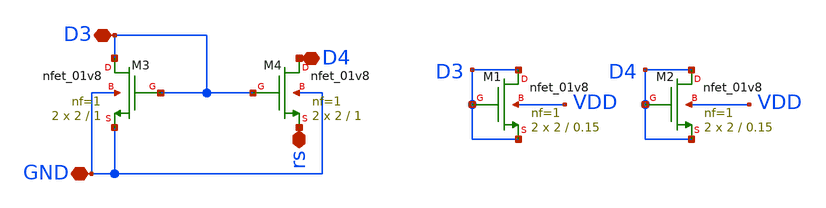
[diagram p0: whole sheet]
** sch_path: opamp/mag/untitled.sch
**.subckt untitled rs D3 GND D4
*.iopin rs
*.iopin D3
*.iopin GND
*.iopin D4
XM4 D4 D3 rs GND sky130_fd_pr__nfet_01v8 L=1 W=2 nf=1 ad='int((nf+1)/2) * W/nf * 0.29' as='int((nf+2)/2) * W/nf * 0.29'
+ pd='2*int((nf+1)/2) * (W/nf + 0.29)' ps='2*int((nf+2)/2) * (W/nf + 0.29)' nrd='0.29 / W' nrs='0.29 / W'
+ sa=0 sb=0 sd=0 mult=2 m=2
XM3 D3 D3 GND GND sky130_fd_pr__nfet_01v8 L=1 W=2 nf=1 ad='int((nf+1)/2) * W/nf * 0.29' as='int((nf+2)/2) * W/nf * 0.29'
+ pd='2*int((nf+1)/2) * (W/nf + 0.29)' ps='2*int((nf+2)/2) * (W/nf + 0.29)' nrd='0.29 / W' nrs='0.29 / W'
+ sa=0 sb=0 sd=0 mult=2 m=2
XM1 D3 D3 D3 VDD sky130_fd_pr__nfet_01v8 L=0.15 W=2 nf=1 ad='int((nf+1)/2) * W/nf * 0.29' as='int((nf+2)/2) * W/nf * 0.29'
+ pd='2*int((nf+1)/2) * (W/nf + 0.29)' ps='2*int((nf+2)/2) * (W/nf + 0.29)' nrd='0.29 / W' nrs='0.29 / W'
+ sa=0 sb=0 sd=0 mult=2 m=2
XM2 D4 D4 D4 VDD sky130_fd_pr__nfet_01v8 L=0.15 W=2 nf=1 ad='int((nf+1)/2) * W/nf * 0.29' as='int((nf+2)/2) * W/nf * 0.29'
+ pd='2*int((nf+1)/2) * (W/nf + 0.29)' ps='2*int((nf+2)/2) * (W/nf + 0.29)' nrd='0.29 / W' nrs='0.29 / W'
+ sa=0 sb=0 sd=0 mult=2 m=2
**.ends
.end
